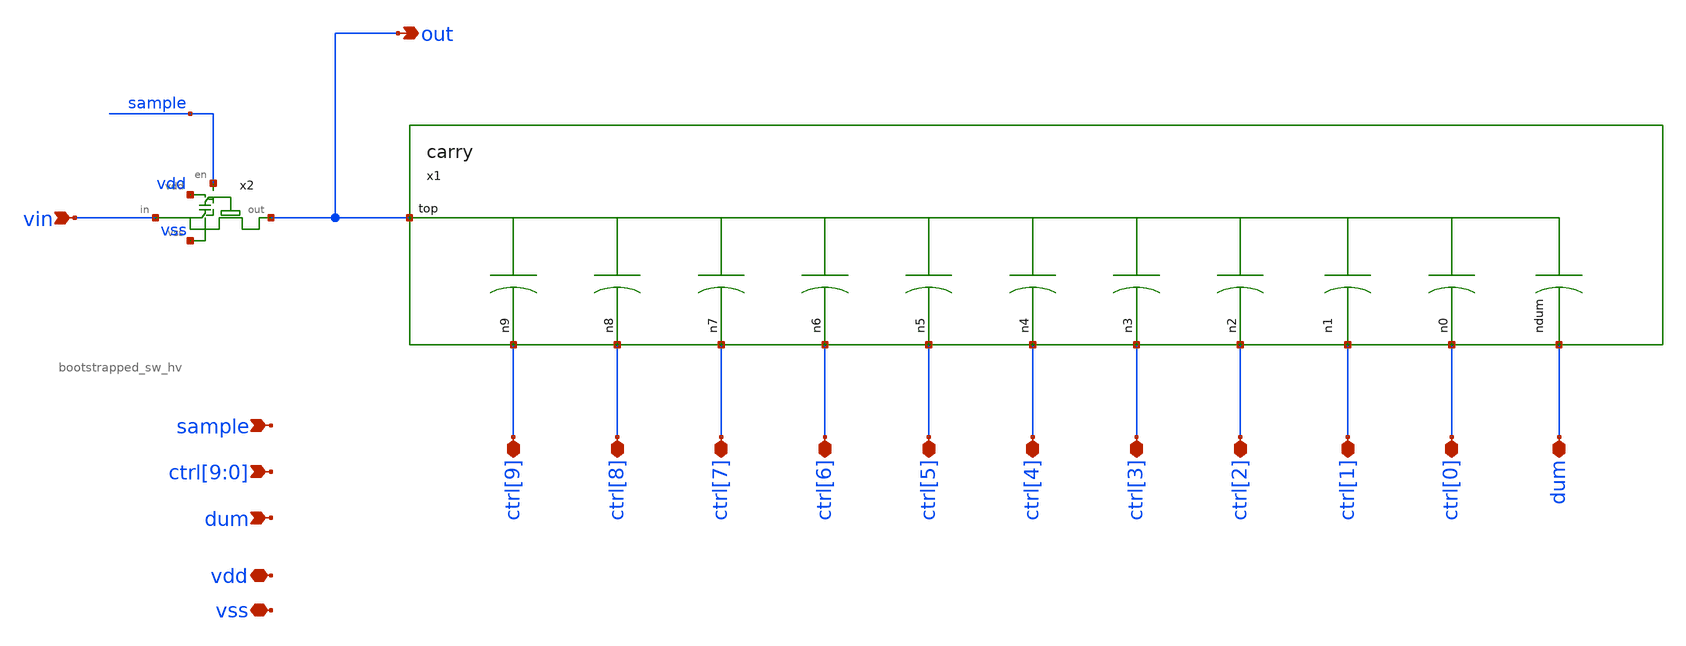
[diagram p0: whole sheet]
** sch_path: xschem/adc/dac.sch
**.subckt dac dum ctrl[0] ctrl[1] ctrl[2] ctrl[3] ctrl[4] ctrl[5] ctrl[6] ctrl[7] ctrl[8] ctrl[9]
*+ out vin sample ctrl[9],ctrl[8],ctrl[7],ctrl[6],ctrl[5],ctrl[4],ctrl[3],ctrl[2],ctrl[1],ctrl[0] dum vdd
*+ vss
*.iopin dum
*.iopin ctrl[0]
*.iopin ctrl[1]
*.iopin ctrl[2]
*.iopin ctrl[3]
*.iopin ctrl[4]
*.iopin ctrl[5]
*.iopin ctrl[6]
*.iopin ctrl[7]
*.iopin ctrl[8]
*.iopin ctrl[9]
*.opin out
*.ipin vin
*.ipin sample
*.ipin ctrl[9],ctrl[8],ctrl[7],ctrl[6],ctrl[5],ctrl[4],ctrl[3],ctrl[2],ctrl[1],ctrl[0]
*.ipin dum
*.iopin vdd
*.iopin vss
x1 out ctrl[6] ctrl[0] ctrl[5] ctrl[4] ctrl[2] dum ctrl[3] ctrl[1] ctrl[7] ctrl[8] ctrl[9] carry
x2 out sample vdd vin vss bootstrapped_sw_hv
**.ends
.end
